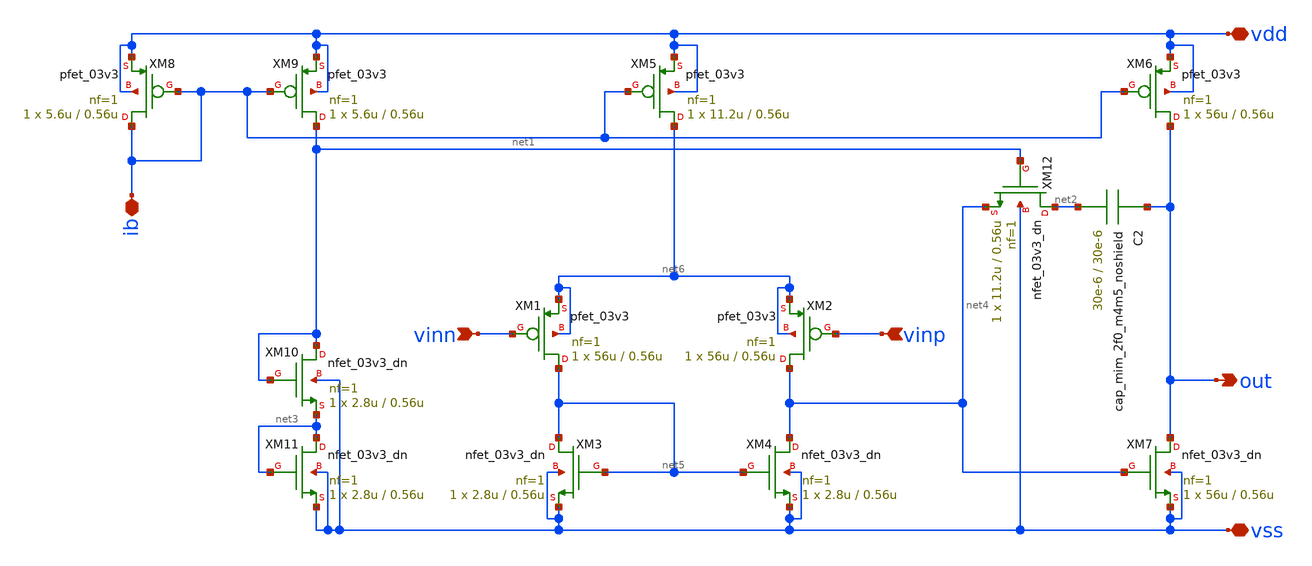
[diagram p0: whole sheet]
** sch_path: noritsuna/ldo/opamp_lvs.sch
**.subckt opamp_lvs vdd ib out vss vinn vinp
*.iopin vdd
*.iopin ib
*.opin out
*.iopin vss
*.ipin vinn
*.ipin vinp
XM9 net1 ib vdd vdd pfet_03v3 L=0.56u W=5.6u nf=1 ad='int((nf+1)/2) * W/nf * 0.18u' as='int((nf+2)/2) * W/nf * 0.18u'
+ pd='2*int((nf+1)/2) * (W/nf + 0.18u)' ps='2*int((nf+2)/2) * (W/nf + 0.18u)' nrd='0.18u / W' nrs='0.18u / W'
+ sa=0 sb=0 sd=0 m=1
XM11 net3 net3 vss vss nfet_03v3_dn L=0.56u W=2.8u nf=1 ad='int((nf+1)/2) * W/nf * 0.18u' as='int((nf+2)/2) * W/nf * 0.18u'
+ pd='2*int((nf+1)/2) * (W/nf + 0.18u)' ps='2*int((nf+2)/2) * (W/nf + 0.18u)' nrd='0.18u / W' nrs='0.18u / W'
+ sa=0 sb=0 sd=0 m=1
XM10 net1 net1 net3 vss nfet_03v3_dn L=0.56u W=2.8u nf=1 ad='int((nf+1)/2) * W/nf * 0.18u' as='int((nf+2)/2) * W/nf * 0.18u'
+ pd='2*int((nf+1)/2) * (W/nf + 0.18u)' ps='2*int((nf+2)/2) * (W/nf + 0.18u)' nrd='0.18u / W' nrs='0.18u / W'
+ sa=0 sb=0 sd=0 m=1
XM12 net2 net1 net4 vss nfet_03v3_dn L=0.56u W=11.2u nf=1 ad='int((nf+1)/2) * W/nf * 0.18u' as='int((nf+2)/2) * W/nf * 0.18u'
+ pd='2*int((nf+1)/2) * (W/nf + 0.18u)' ps='2*int((nf+2)/2) * (W/nf + 0.18u)' nrd='0.18u / W' nrs='0.18u / W'
+ sa=0 sb=0 sd=0 m=1
XM8 ib ib vdd vdd pfet_03v3 L=0.56u W=5.6u nf=1 ad='int((nf+1)/2) * W/nf * 0.18u' as='int((nf+2)/2) * W/nf * 0.18u'
+ pd='2*int((nf+1)/2) * (W/nf + 0.18u)' ps='2*int((nf+2)/2) * (W/nf + 0.18u)' nrd='0.18u / W' nrs='0.18u / W'
+ sa=0 sb=0 sd=0 m=1
XM6 out ib vdd vdd pfet_03v3 L=0.56u W=56u nf=1 ad='int((nf+1)/2) * W/nf * 0.18u' as='int((nf+2)/2) * W/nf * 0.18u'
+ pd='2*int((nf+1)/2) * (W/nf + 0.18u)' ps='2*int((nf+2)/2) * (W/nf + 0.18u)' nrd='0.18u / W' nrs='0.18u / W'
+ sa=0 sb=0 sd=0 m=1
XM7 out net4 vss vss nfet_03v3_dn L=0.56u W=56u nf=1 ad='int((nf+1)/2) * W/nf * 0.18u' as='int((nf+2)/2) * W/nf * 0.18u'
+ pd='2*int((nf+1)/2) * (W/nf + 0.18u)' ps='2*int((nf+2)/2) * (W/nf + 0.18u)' nrd='0.18u / W' nrs='0.18u / W'
+ sa=0 sb=0 sd=0 m=1
XM1 net5 vinn net6 net6 pfet_03v3 L=0.56u W=56u nf=1 ad='int((nf+1)/2) * W/nf * 0.18u' as='int((nf+2)/2) * W/nf * 0.18u'
+ pd='2*int((nf+1)/2) * (W/nf + 0.18u)' ps='2*int((nf+2)/2) * (W/nf + 0.18u)' nrd='0.18u / W' nrs='0.18u / W'
+ sa=0 sb=0 sd=0 m=1
XM2 net4 vinp net6 net6 pfet_03v3 L=0.56u W=56u nf=1 ad='int((nf+1)/2) * W/nf * 0.18u' as='int((nf+2)/2) * W/nf * 0.18u'
+ pd='2*int((nf+1)/2) * (W/nf + 0.18u)' ps='2*int((nf+2)/2) * (W/nf + 0.18u)' nrd='0.18u / W' nrs='0.18u / W'
+ sa=0 sb=0 sd=0 m=1
XM5 net6 ib vdd vdd pfet_03v3 L=0.56u W=11.2u nf=1 ad='int((nf+1)/2) * W/nf * 0.18u' as='int((nf+2)/2) * W/nf * 0.18u'
+ pd='2*int((nf+1)/2) * (W/nf + 0.18u)' ps='2*int((nf+2)/2) * (W/nf + 0.18u)' nrd='0.18u / W' nrs='0.18u / W'
+ sa=0 sb=0 sd=0 m=1
XM4 net4 net5 vss vss nfet_03v3_dn L=0.56u W=2.8u nf=1 ad='int((nf+1)/2) * W/nf * 0.18u' as='int((nf+2)/2) * W/nf * 0.18u'
+ pd='2*int((nf+1)/2) * (W/nf + 0.18u)' ps='2*int((nf+2)/2) * (W/nf + 0.18u)' nrd='0.18u / W' nrs='0.18u / W'
+ sa=0 sb=0 sd=0 m=1
XM3 net5 net5 vss vss nfet_03v3_dn L=0.56u W=2.8u nf=1 ad='int((nf+1)/2) * W/nf * 0.18u' as='int((nf+2)/2) * W/nf * 0.18u'
+ pd='2*int((nf+1)/2) * (W/nf + 0.18u)' ps='2*int((nf+2)/2) * (W/nf + 0.18u)' nrd='0.18u / W' nrs='0.18u / W'
+ sa=0 sb=0 sd=0 m=1
C2 out net2 cap_mim_2f0_m4m5_noshield W=30e-6 L=30e-6
**.ends
.end
